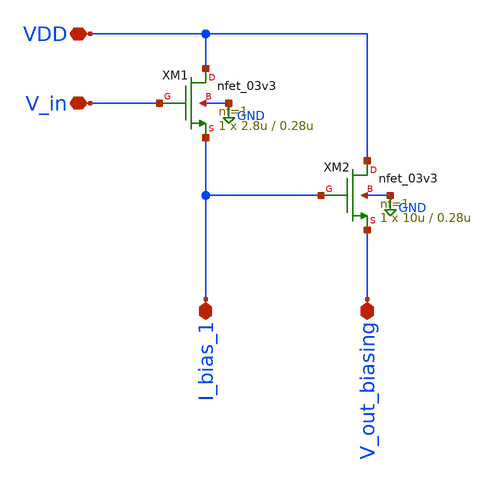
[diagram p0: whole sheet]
** sch_path: src/design_xsch/Output_stage.sch
**.subckt Output_stage VDD V_in I_bias_1 V_out_biasing
*.iopin VDD
*.iopin V_in
*.iopin I_bias_1
*.iopin V_out_biasing
XM1 VDD V_in I_bias_1 GND nfet_03v3 L=0.28u W=2.8u nf=1 ad='int((nf+1)/2) * W/nf * 0.18u' as='int((nf+2)/2) * W/nf * 0.18u'
+ pd='2*int((nf+1)/2) * (W/nf + 0.18u)' ps='2*int((nf+2)/2) * (W/nf + 0.18u)' nrd='0.18u / W' nrs='0.18u / W'
+ sa=0 sb=0 sd=0 m=1
XM2 VDD I_bias_1 V_out_biasing GND nfet_03v3 L=0.28u W=10u nf=1 ad='int((nf+1)/2) * W/nf * 0.18u' as='int((nf+2)/2) * W/nf * 0.18u'
+ pd='2*int((nf+1)/2) * (W/nf + 0.18u)' ps='2*int((nf+2)/2) * (W/nf + 0.18u)' nrd='0.18u / W' nrs='0.18u / W'
+ sa=0 sb=0 sd=0 m=1
**.ends
.GLOBAL GND
.end
